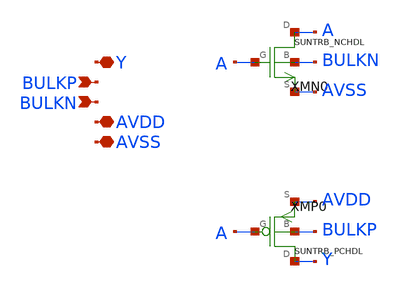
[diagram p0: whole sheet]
** sch_path: ip/sun_trb_sky130nm/design/SUN_TRB_SKY130NM/SUNTRB_TIEH_CV.sch
**.subckt SUNTRB_TIEH_CV Y BULKP BULKN AVDD AVSS
*.iopin Y
*.ipin BULKP
*.ipin BULKN
*.iopin AVDD
*.iopin AVSS
XMN0 A A AVSS BULKN SUNTRB_NCHDL xoffset=0 yoffset=0 angle=0
XMP0 Y A AVDD BULKP SUNTRB_PCHDL xoffset=0 yoffset=0 angle=0
**.ends
.end
